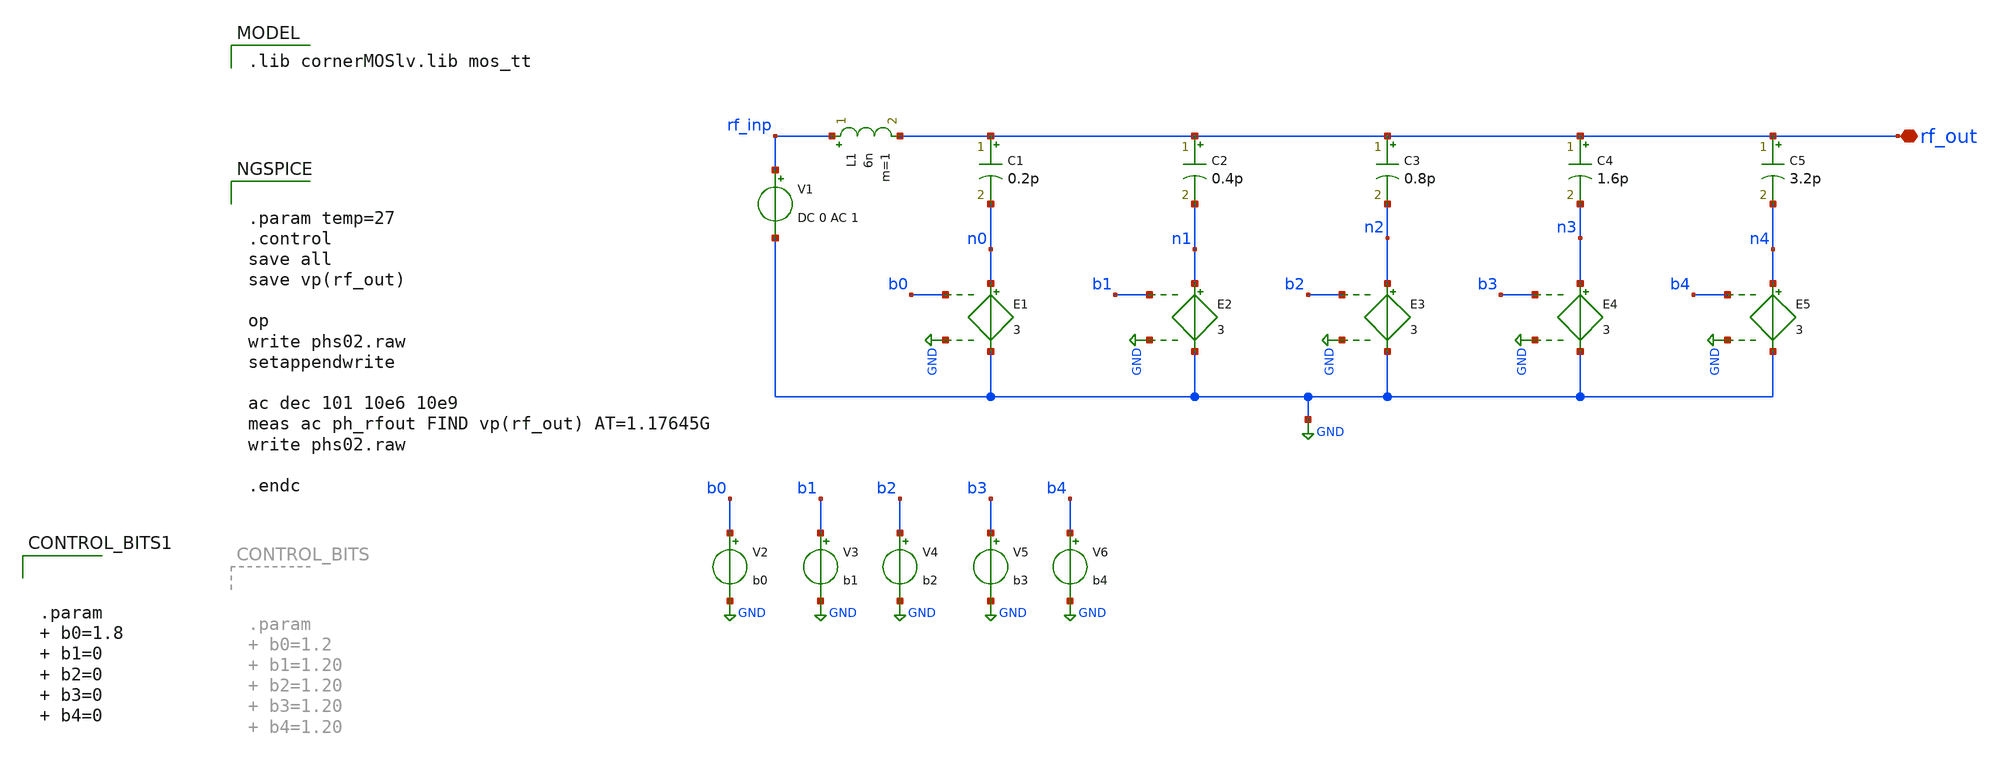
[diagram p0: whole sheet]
** sch_path: xschem/phs02.sch
**.subckt phs02 rf_out
*.iopin rf_out
L1 rf_inp rf_out 6n m=1
C1 rf_out n0 0.2p m=1
C2 rf_out n1 0.4p m=1
C3 rf_out n2 0.8p m=1
C4 rf_out n3 1.6p m=1
C5 rf_out n4 3.2p m=1
V1 rf_inp GND DC 0 AC 1
V2 b0 GND b0
V3 b1 GND b1
V4 b2 GND b2
V5 b3 GND b3
V6 b4 GND b4
E1 n0 GND b0 GND 3
E2 n1 GND b1 GND 3
E3 n2 GND b2 GND 3
E4 n3 GND b3 GND 3
E5 n4 GND b4 GND 3
**** begin user architecture code
 .lib cornerMOSlv.lib mos_tt



.param temp=27
.control
save all
save vp(rf_out)

op
write phs02.raw
setappendwrite

ac dec 101 10e6 10e9
meas ac ph_rfout FIND vp(rf_out) AT=1.17645G
write phs02.raw

.endc





.param   b0=1.8  b1=0  b2=0  b3=0  b4=0


**** end user architecture code
**.ends
.GLOBAL GND
.end
